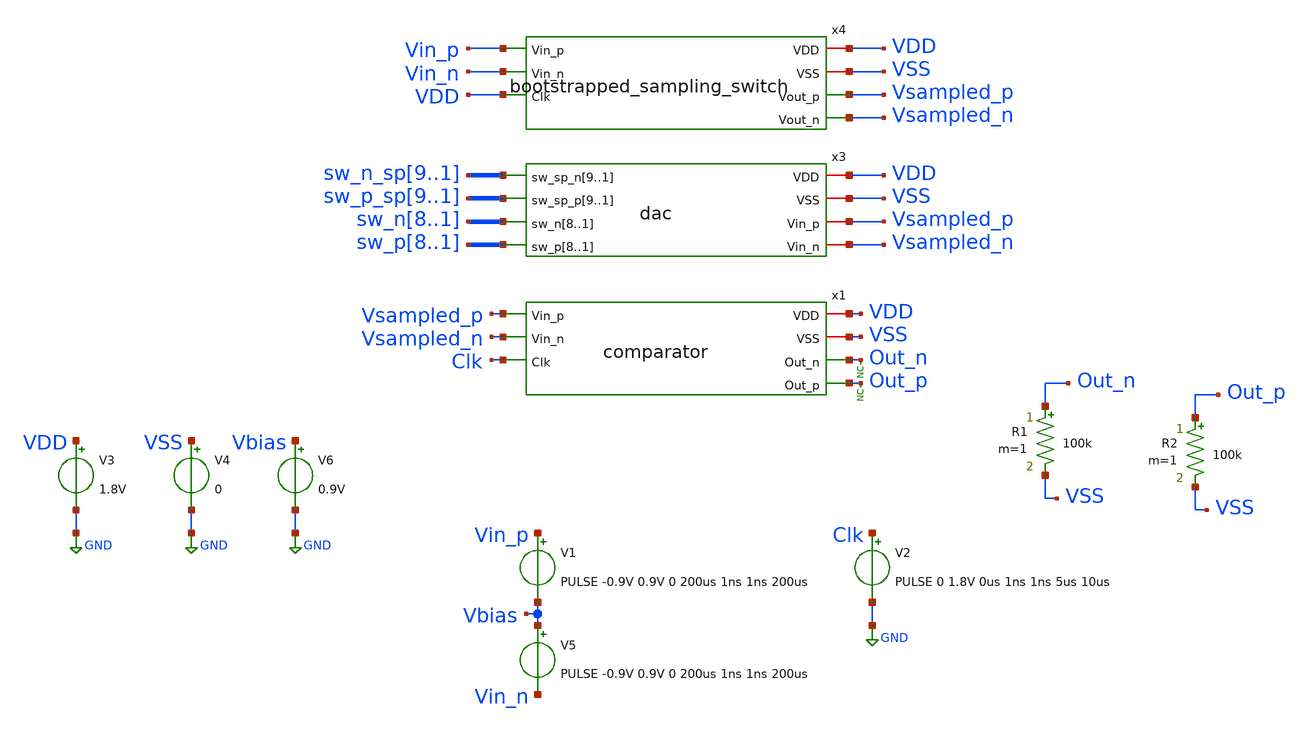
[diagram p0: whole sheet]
** sch_path: xschem/tests/comparator/comparator_dac_sw_test.sch
**.subckt comparator_dac_sw_test
V3 VDD GND 1.8V
V4 VSS GND 0
x1 VDD VSS Vsampled_p Out_n Vsampled_n Out_p Clk comparator
V1 Vin_p Vbias PULSE -0.9V 0.9V 0 200us 1ns 1ns 200us
V2 Clk GND PULSE 0 1.8V 0us 1ns 1ns 5us 10us
* noconn Out_p
* noconn Out_n
V5 Vbias Vin_n PULSE -0.9V 0.9V 0 200us 1ns 1ns 200us
V6 Vbias GND 0.9V
R1 Out_n VSS 100k m=1
R2 Out_p VSS 100k m=1
x3 sw_n_sp9 sw_n_sp8 sw_n_sp7 sw_n_sp6 sw_n_sp5 sw_n_sp4 sw_n_sp3 sw_n_sp2 sw_n_sp1 VDD sw_p_sp9
+ sw_p_sp8 sw_p_sp7 sw_p_sp6 sw_p_sp5 sw_p_sp4 sw_p_sp3 sw_p_sp2 sw_p_sp1 VSS sw_n8 sw_n7 sw_n6 sw_n5 sw_n4
+ sw_n3 sw_n2 sw_n1 Vsampled_p sw_p8 sw_p7 sw_p6 sw_p5 sw_p4 sw_p3 sw_p2 sw_p1 Vsampled_n dac
x4 VDD Vin_p VSS Vin_n VDD Vsampled_p Vsampled_n bootstrapped_sampling_switch
**** begin user architecture code
 .lib $::SKYWATER_MODELS/sky130.lib.spice tt
.include $::SKYWATER_STDCELLS/sky130_fd_sc_hd.spice


.options acct list
.temp 25
*vvcc VDD 0 dc 1.8
*vvss VSS 0 0

v_sp_n1 sw_sp_n1 gnd 1.8V
v_sp_n2 sw_sp_n2 gnd 1.8V
v_sp_n3 sw_sp_n3 gnd 1.8V
v_sp_n4 sw_sp_n4 gnd 1.8V
v_sp_n5 sw_sp_n5 gnd 1.8V
v_sp_n6 sw_sp_n6 gnd 1.8V
v_sp_n7 sw_sp_n7 gnd 1.8V
v_sp_n8 sw_sp_n8 gnd 1.8V
v_sp_n9 sw_sp_n9 gnd 1.8V

v_n1 sw_n1 gnd 0
v_n2 sw_n2 gnd 0
v_n3 sw_n3 gnd 0
v_n4 sw_n4 gnd 0
v_n5 sw_n5 gnd 0
v_n6 sw_n6 gnd 0
v_n7 sw_n7 gnd 0
v_n8 sw_n8 gnd 0

v_sp_p1 sw_sp_p1 gnd 1.8V
v_sp_p2 sw_sp_p2 gnd 1.8V
v_sp_p3 sw_sp_p3 gnd 1.8V
v_sp_p4 sw_sp_p4 gnd 1.8V
v_sp_p5 sw_sp_p5 gnd 1.8V
v_sp_p6 sw_sp_p6 gnd 1.8V
v_sp_p7 sw_sp_p7 gnd 1.8V
v_sp_p8 sw_sp_p8 gnd 1.8V
v_sp_p9 sw_sp_p9 gnd 1.8V

v_p1 sw_p1 gnd 0
v_p2 sw_p2 gnd 0
v_p3 sw_p3 gnd 0
v_p4 sw_p4 gnd 0
v_p5 sw_p5 gnd 0
v_p6 sw_p6 gnd 0
v_p7 sw_p7 gnd 0
v_p8 sw_p8 gnd 0
.control
save all
tran 0.1u 200u
*dc V1 0 1.8V 0.1
plot Vin_p-Vin_n Out_p-Out_n Clk-4
plot Vin_p-Vin_n x1.pre_amp_p-x1.pre_amp_n Clk-4
write comparator_dac_sw_test.raw
.endc


**** end user architecture code
**.ends
.GLOBAL GND
.end
